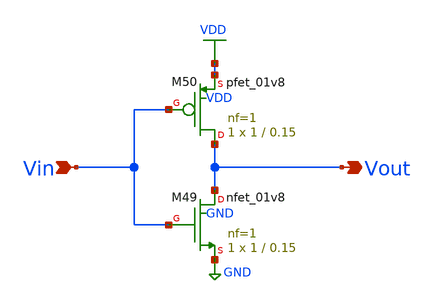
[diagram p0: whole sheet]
** sch_path: xschem/Standard Cells/Inverter.sch
**.subckt Inverter Vout Vin
*.opin Vout
*.ipin Vin
XM49 Vout Vin GND GND sky130_fd_pr__nfet_01v8 L=0.15 W=1 nf=1 ad='int((nf+1)/2) * W/nf * 0.29' as='int((nf+2)/2) * W/nf * 0.29'
+ pd='2*int((nf+1)/2) * (W/nf + 0.29)' ps='2*int((nf+2)/2) * (W/nf + 0.29)' nrd='0.29 / W' nrs='0.29 / W'
+ sa=0 sb=0 sd=0 mult=1 m=1
XM50 Vout Vin VDD VDD sky130_fd_pr__pfet_01v8 L=0.15 W=1 nf=1 ad='int((1 + 1)/2) * 1 / 1 * 0.29' as='int((1 + 2)/2) * 1 / 1 * 0.29'
+ pd='2*int((1 + 1)/2) * (1 / 1 + 0.29)' ps='2*int((1 + 2)/2) * (1 / 1 + 0.29)' nrd='0.29 / 1 ' nrs='0.29 / 1 '
+ sa=0 sb=0 sd=0 mult=1 m=1
**.ends
.GLOBAL GND
.GLOBAL VDD
.end
